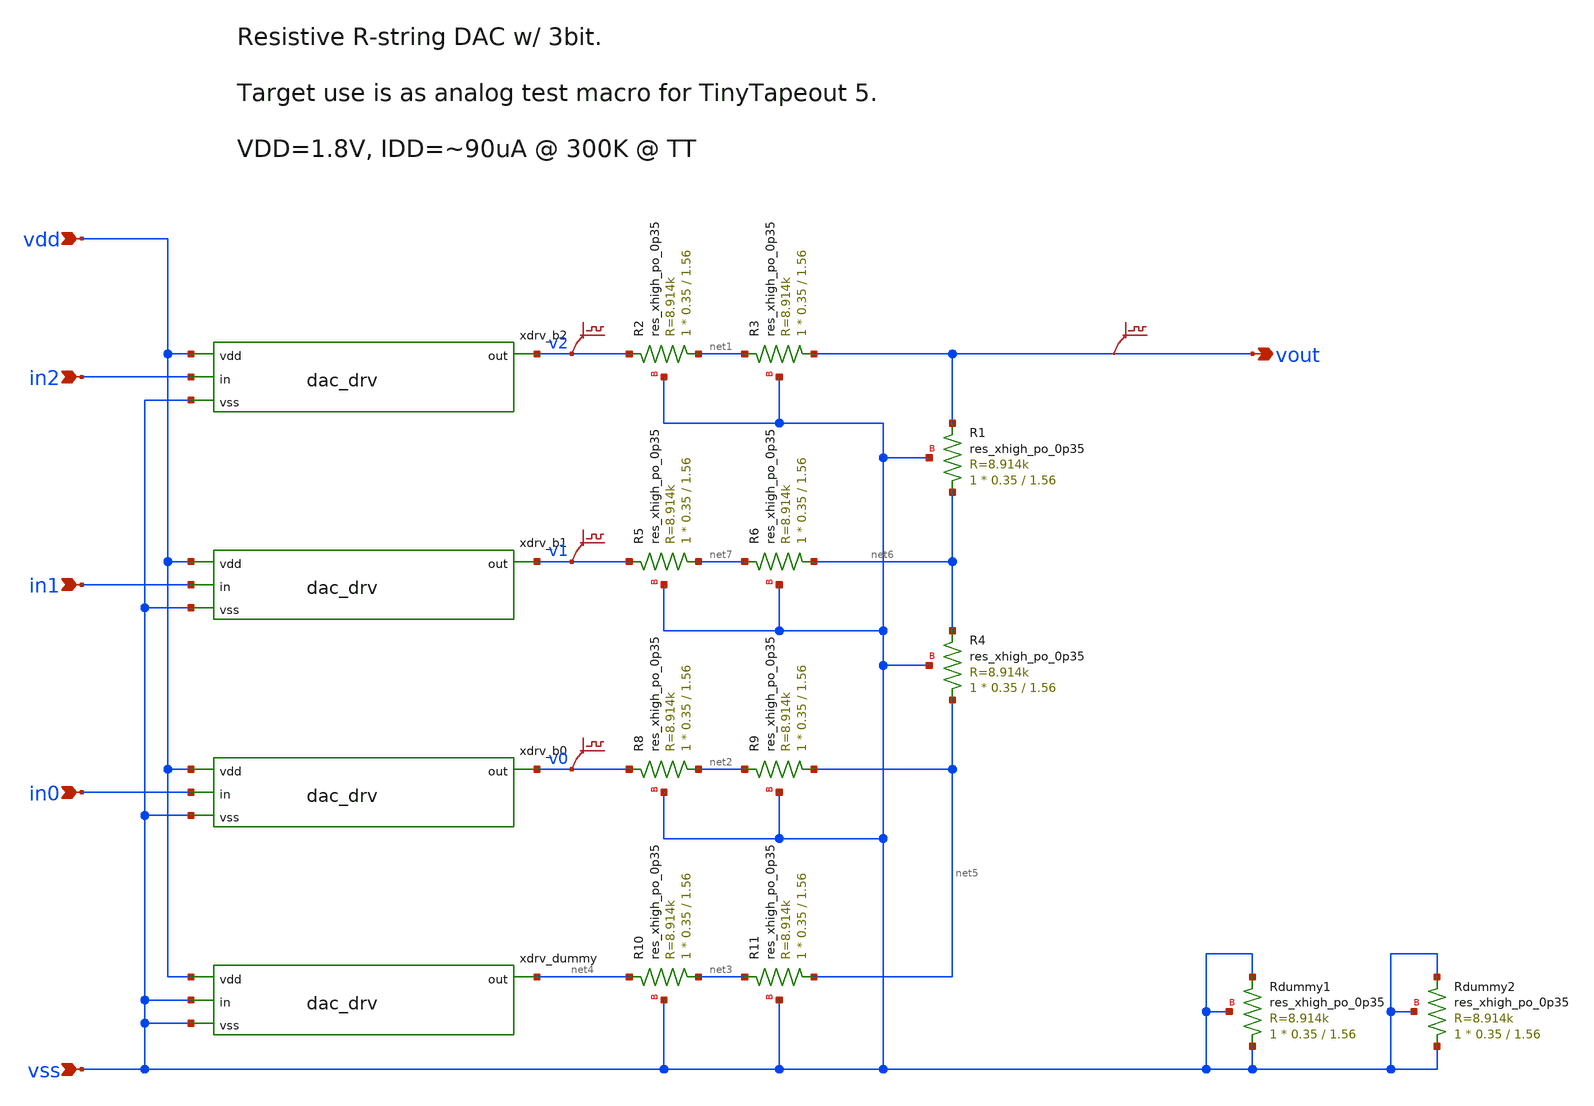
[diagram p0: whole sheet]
** sch_path: xschem/dac.sch
**.subckt dac vdd vss vout in0 in1 in2
*.ipin vdd
*.ipin vss
*.opin vout
*.ipin in0
*.ipin in1
*.ipin in2
xdrv_b2 vdd in2 v2 vss dac_drv
xdrv_b1 vdd in1 v1 vss dac_drv
xdrv_b0 vdd in0 v0 vss dac_drv
XR1 net6 vout vss sky130_fd_pr__res_xhigh_po_0p35 L=1.56 mult=1 m=1
xdrv_dummy vdd vss net4 vss dac_drv
XR2 net1 v2 vss sky130_fd_pr__res_xhigh_po_0p35 L=1.56 mult=1 m=1
XR3 vout net1 vss sky130_fd_pr__res_xhigh_po_0p35 L=1.56 mult=1 m=1
.save v(vout)
.save v(v2)
.save v(v1)
.save v(v0)
XR4 net5 net6 vss sky130_fd_pr__res_xhigh_po_0p35 L=1.56 mult=1 m=1
XR5 net7 v1 vss sky130_fd_pr__res_xhigh_po_0p35 L=1.56 mult=1 m=1
XR6 net6 net7 vss sky130_fd_pr__res_xhigh_po_0p35 L=1.56 mult=1 m=1
XR8 net2 v0 vss sky130_fd_pr__res_xhigh_po_0p35 L=1.56 mult=1 m=1
XR9 net5 net2 vss sky130_fd_pr__res_xhigh_po_0p35 L=1.56 mult=1 m=1
XR10 net3 net4 vss sky130_fd_pr__res_xhigh_po_0p35 L=1.56 mult=1 m=1
XR11 net5 net3 vss sky130_fd_pr__res_xhigh_po_0p35 L=1.56 mult=1 m=1
XRdummy1 vss vss vss sky130_fd_pr__res_xhigh_po_0p35 L=1.56 mult=1 m=1
XRdummy2 vss vss vss sky130_fd_pr__res_xhigh_po_0p35 L=1.56 mult=1 m=1
**.ends

* expanding   symbol:  dac_drv.sym # of pins=4
** sym_path: dac_drv.sym
** sch_path: dac_drv.sch
.subckt dac_drv vdd in out vss
*.ipin vdd
*.ipin vss
*.ipin in
*.opin out
XM1 net1 in vss vss sky130_fd_pr__nfet_01v8 L=0.5 W=5 nf=1 ad='int((nf+1)/2) * W/nf * 0.29' as='int((nf+2)/2) * W/nf * 0.29'
+ pd='2*int((nf+1)/2) * (W/nf + 0.29)' ps='2*int((nf+2)/2) * (W/nf + 0.29)' nrd='0.29 / W' nrs='0.29 / W'
+ sa=0 sb=0 sd=0 mult=1 m=1
XM2A net1 in vdd vdd sky130_fd_pr__pfet_01v8 L=0.5 W=5 nf=1 ad='int((nf+1)/2) * W/nf * 0.29' as='int((nf+2)/2) * W/nf * 0.29'
+ pd='2*int((nf+1)/2) * (W/nf + 0.29)' ps='2*int((nf+2)/2) * (W/nf + 0.29)' nrd='0.29 / W' nrs='0.29 / W'
+ sa=0 sb=0 sd=0 mult=1 m=1
XM4A out net1 vdd vdd sky130_fd_pr__pfet_01v8 L=0.5 W=5 nf=1 ad='int((nf+1)/2) * W/nf * 0.29' as='int((nf+2)/2) * W/nf * 0.29'
+ pd='2*int((nf+1)/2) * (W/nf + 0.29)' ps='2*int((nf+2)/2) * (W/nf + 0.29)' nrd='0.29 / W' nrs='0.29 / W'
+ sa=0 sb=0 sd=0 mult=1 m=1
XM3 out net1 vss vss sky130_fd_pr__nfet_01v8 L=0.5 W=5 nf=1 ad='int((nf+1)/2) * W/nf * 0.29' as='int((nf+2)/2) * W/nf * 0.29'
+ pd='2*int((nf+1)/2) * (W/nf + 0.29)' ps='2*int((nf+2)/2) * (W/nf + 0.29)' nrd='0.29 / W' nrs='0.29 / W'
+ sa=0 sb=0 sd=0 mult=1 m=1
XM2B net1 in vdd vdd sky130_fd_pr__pfet_01v8 L=0.5 W=5 nf=1 ad='int((nf+1)/2) * W/nf * 0.29' as='int((nf+2)/2) * W/nf * 0.29'
+ pd='2*int((nf+1)/2) * (W/nf + 0.29)' ps='2*int((nf+2)/2) * (W/nf + 0.29)' nrd='0.29 / W' nrs='0.29 / W'
+ sa=0 sb=0 sd=0 mult=1 m=1
XM4B out net1 vdd vdd sky130_fd_pr__pfet_01v8 L=0.5 W=5 nf=1 ad='int((nf+1)/2) * W/nf * 0.29' as='int((nf+2)/2) * W/nf * 0.29'
+ pd='2*int((nf+1)/2) * (W/nf + 0.29)' ps='2*int((nf+2)/2) * (W/nf + 0.29)' nrd='0.29 / W' nrs='0.29 / W'
+ sa=0 sb=0 sd=0 mult=1 m=1
.ends

.end
